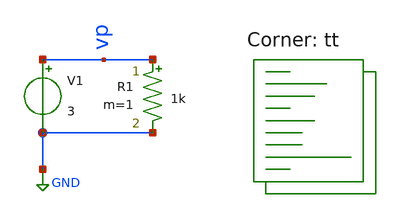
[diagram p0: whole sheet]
** sch_path: Schematics/test_graphs.sch
**.subckt test_graphs
V1 vp GND 3
R1 vp GND 1k m=1
**** begin user architecture code
.lib $::SKYWATER_MODELS/sky130.lib.spice tt
**** end user architecture code
**.ends
.GLOBAL GND
**** begin user architecture code

.options savecurrents
.tran 100n 1m uic
.save all
.control
	run
	write test_graphs.raw
*plot all.Vout
.endc


**** end user architecture code
.end
